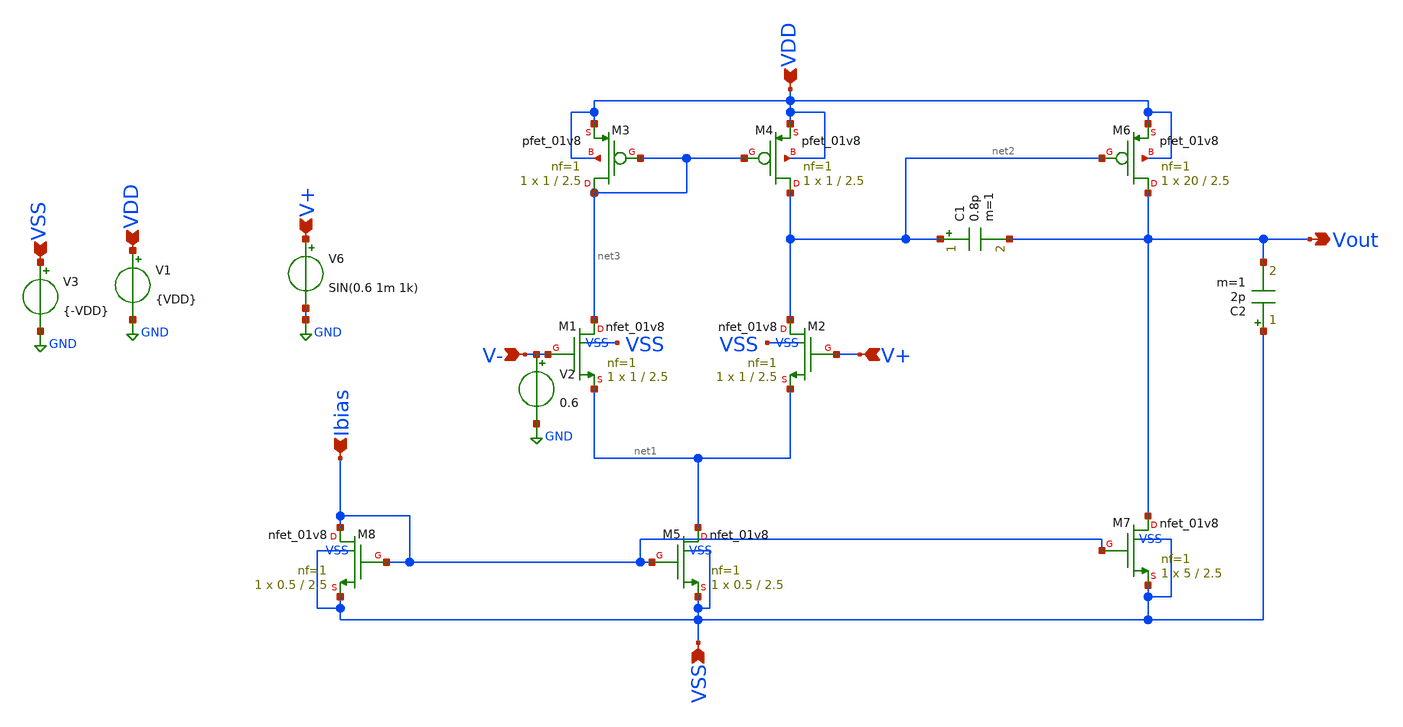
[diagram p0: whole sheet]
** sch_path: xschem/EA/2stageCMOSOpAmp-copy.sch
**.subckt 2stageCMOSOpAmp-copy VDD VSS Vout V+ V- Ibias VDD V+ VSS
*.ipin VDD
*.ipin VSS
*.opin Vout
*.ipin V+
*.ipin V-
*.ipin Ibias
*.ipin VDD
*.ipin V+
*.ipin VSS
C1 net2 Vout 0.8p m=1
C2 VSS Vout 2p m=1
XM1 net3 V- net1 VSS sky130_fd_pr__nfet_01v8 L=2.5 W=1 nf=1 ad='int((nf+1)/2) * W/nf * 0.29' as='int((nf+2)/2) * W/nf * 0.29'
+ pd='2*int((nf+1)/2) * (W/nf + 0.29)' ps='2*int((nf+2)/2) * (W/nf + 0.29)' nrd='0.29 / W' nrs='0.29 / W'
+ sa=0 sb=0 sd=0 mult=1 m=1
XM2 net2 V+ net1 VSS sky130_fd_pr__nfet_01v8 L=2.5 W=1 nf=1 ad='int((nf+1)/2) * W/nf * 0.29' as='int((nf+2)/2) * W/nf * 0.29'
+ pd='2*int((nf+1)/2) * (W/nf + 0.29)' ps='2*int((nf+2)/2) * (W/nf + 0.29)' nrd='0.29 / W' nrs='0.29 / W'
+ sa=0 sb=0 sd=0 mult=1 m=1
XM3 net3 net3 VDD VDD sky130_fd_pr__pfet_01v8 L=2.5 W=1 nf=1 ad='int((nf+1)/2) * W/nf * 0.29' as='int((nf+2)/2) * W/nf * 0.29'
+ pd='2*int((nf+1)/2) * (W/nf + 0.29)' ps='2*int((nf+2)/2) * (W/nf + 0.29)' nrd='0.29 / W' nrs='0.29 / W'
+ sa=0 sb=0 sd=0 mult=1 m=1
XM4 net2 net3 VDD VDD sky130_fd_pr__pfet_01v8 L=2.5 W=1 nf=1 ad='int((nf+1)/2) * W/nf * 0.29' as='int((nf+2)/2) * W/nf * 0.29'
+ pd='2*int((nf+1)/2) * (W/nf + 0.29)' ps='2*int((nf+2)/2) * (W/nf + 0.29)' nrd='0.29 / W' nrs='0.29 / W'
+ sa=0 sb=0 sd=0 mult=1 m=1
XM6 Vout net2 VDD VDD sky130_fd_pr__pfet_01v8 L=2.5 W=20 nf=1 ad='int((nf+1)/2) * W/nf * 0.29' as='int((nf+2)/2) * W/nf * 0.29'
+ pd='2*int((nf+1)/2) * (W/nf + 0.29)' ps='2*int((nf+2)/2) * (W/nf + 0.29)' nrd='0.29 / W' nrs='0.29 / W'
+ sa=0 sb=0 sd=0 mult=1 m=1
XM5 net1 Ibias VSS VSS sky130_fd_pr__nfet_01v8 L=2.5 W=0.5 nf=1 ad='int((nf+1)/2) * W/nf * 0.29' as='int((nf+2)/2) * W/nf * 0.29'
+ pd='2*int((nf+1)/2) * (W/nf + 0.29)' ps='2*int((nf+2)/2) * (W/nf + 0.29)' nrd='0.29 / W' nrs='0.29 / W'
+ sa=0 sb=0 sd=0 mult=1 m=1
XM8 Ibias Ibias VSS VSS sky130_fd_pr__nfet_01v8 L=2.5 W=0.5 nf=1 ad='int((nf+1)/2) * W/nf * 0.29' as='int((nf+2)/2) * W/nf * 0.29'
+ pd='2*int((nf+1)/2) * (W/nf + 0.29)' ps='2*int((nf+2)/2) * (W/nf + 0.29)' nrd='0.29 / W' nrs='0.29 / W'
+ sa=0 sb=0 sd=0 mult=1 m=1
XM7 Vout Ibias VSS VSS sky130_fd_pr__nfet_01v8 L=2.5 W=5 nf=1 ad='int((nf+1)/2) * W/nf * 0.29' as='int((nf+2)/2) * W/nf * 0.29'
+ pd='2*int((nf+1)/2) * (W/nf + 0.29)' ps='2*int((nf+2)/2) * (W/nf + 0.29)' nrd='0.29 / W' nrs='0.29 / W'
+ sa=0 sb=0 sd=0 mult=1 m=1
V2 V- GND 0.6
V1 VDD GND {VDD}
V6 V+ GND SIN(0.6 1m 1k)
V3 VSS GND {-VDD}
**** begin user architecture code



.lib /usr/local/share/pdk/sky130A/libs.tech/ngspice/sky130.lib.spice tt
.param VDD=1.8 amp=1.2
.tran 5u 5m
*.ac dec 20 1 1e12
.save all

.control
run
plot vout
*plot db(vout/v(v+))
*plot 180*cph(vout)/pi
set wr_singlescale
set wr_vecnames
*wrdata /foss/designs/2stageCMOSOpAmp/sim_data/GainvsFreq/gain(max).txt db(vout/v(v+))
*wrdata /foss/designs/2stageCMOSOpAmp/sim_data/sample_waves/a1.3m_f1k_gain700.txt vout
*wrdata /foss/designs/2stageCMOSOpAmp/sim_data/SR/SR.txt vout

.endc


**** end user architecture code
**.ends
.GLOBAL GND
.end
